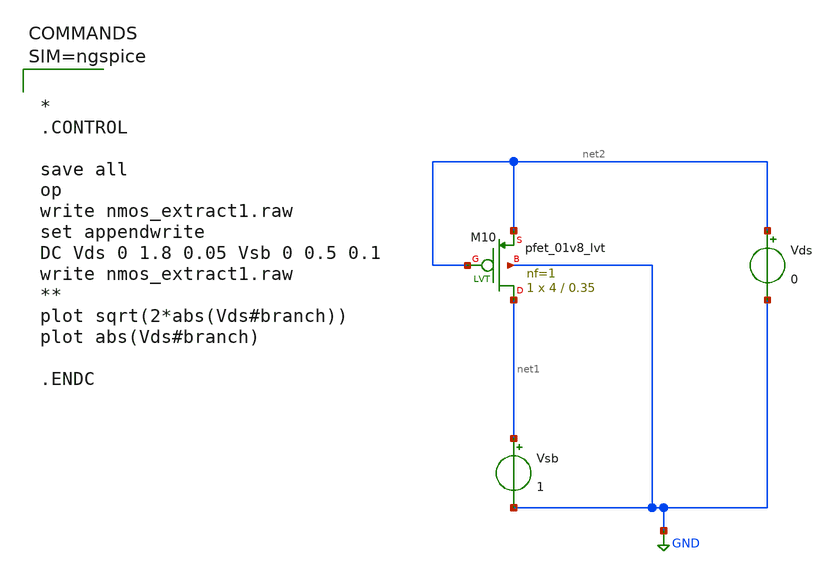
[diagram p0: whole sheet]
** sch_path: work/xschem/nmos_9.sch
**.subckt nmos_9
Vsb net1 GND 1
Vds net2 GND 0
XM10 net1 net2 net2 GND sky130_fd_pr__pfet_01v8_lvt L=0.35 W=4 nf=1 ad='int((1 + 1)/2) * 4 / 1 * 0.29'
+ as='int((1 + 2)/2) * 4 / 1 * 0.29' pd='2*int((1 + 1)/2) * (4 / 1 + 0.29)' ps='2*int((1 + 2)/2) * (4 / 1 + 0.29)'
+ nrd='0.29 / 4 ' nrs='0.29 / 4 ' sa=0 sb=0 sd=0 mult=1 m=1
**** begin user architecture code



*
.CONTROL

save all
op
write nmos_extract1.raw
set appendwrite
DC Vds 0 1.8 0.05 Vsb 0 0.5 0.1
write nmos_extract1.raw
**
plot sqrt(2*abs(Vds#branch))
plot abs(Vds#branch)

.ENDC




** opencircuitdesign pdks install
.lib $::SKYWATER_MODELS/sky130.lib.spice tt

**** end user architecture code
**.ends
.GLOBAL GND
.end
